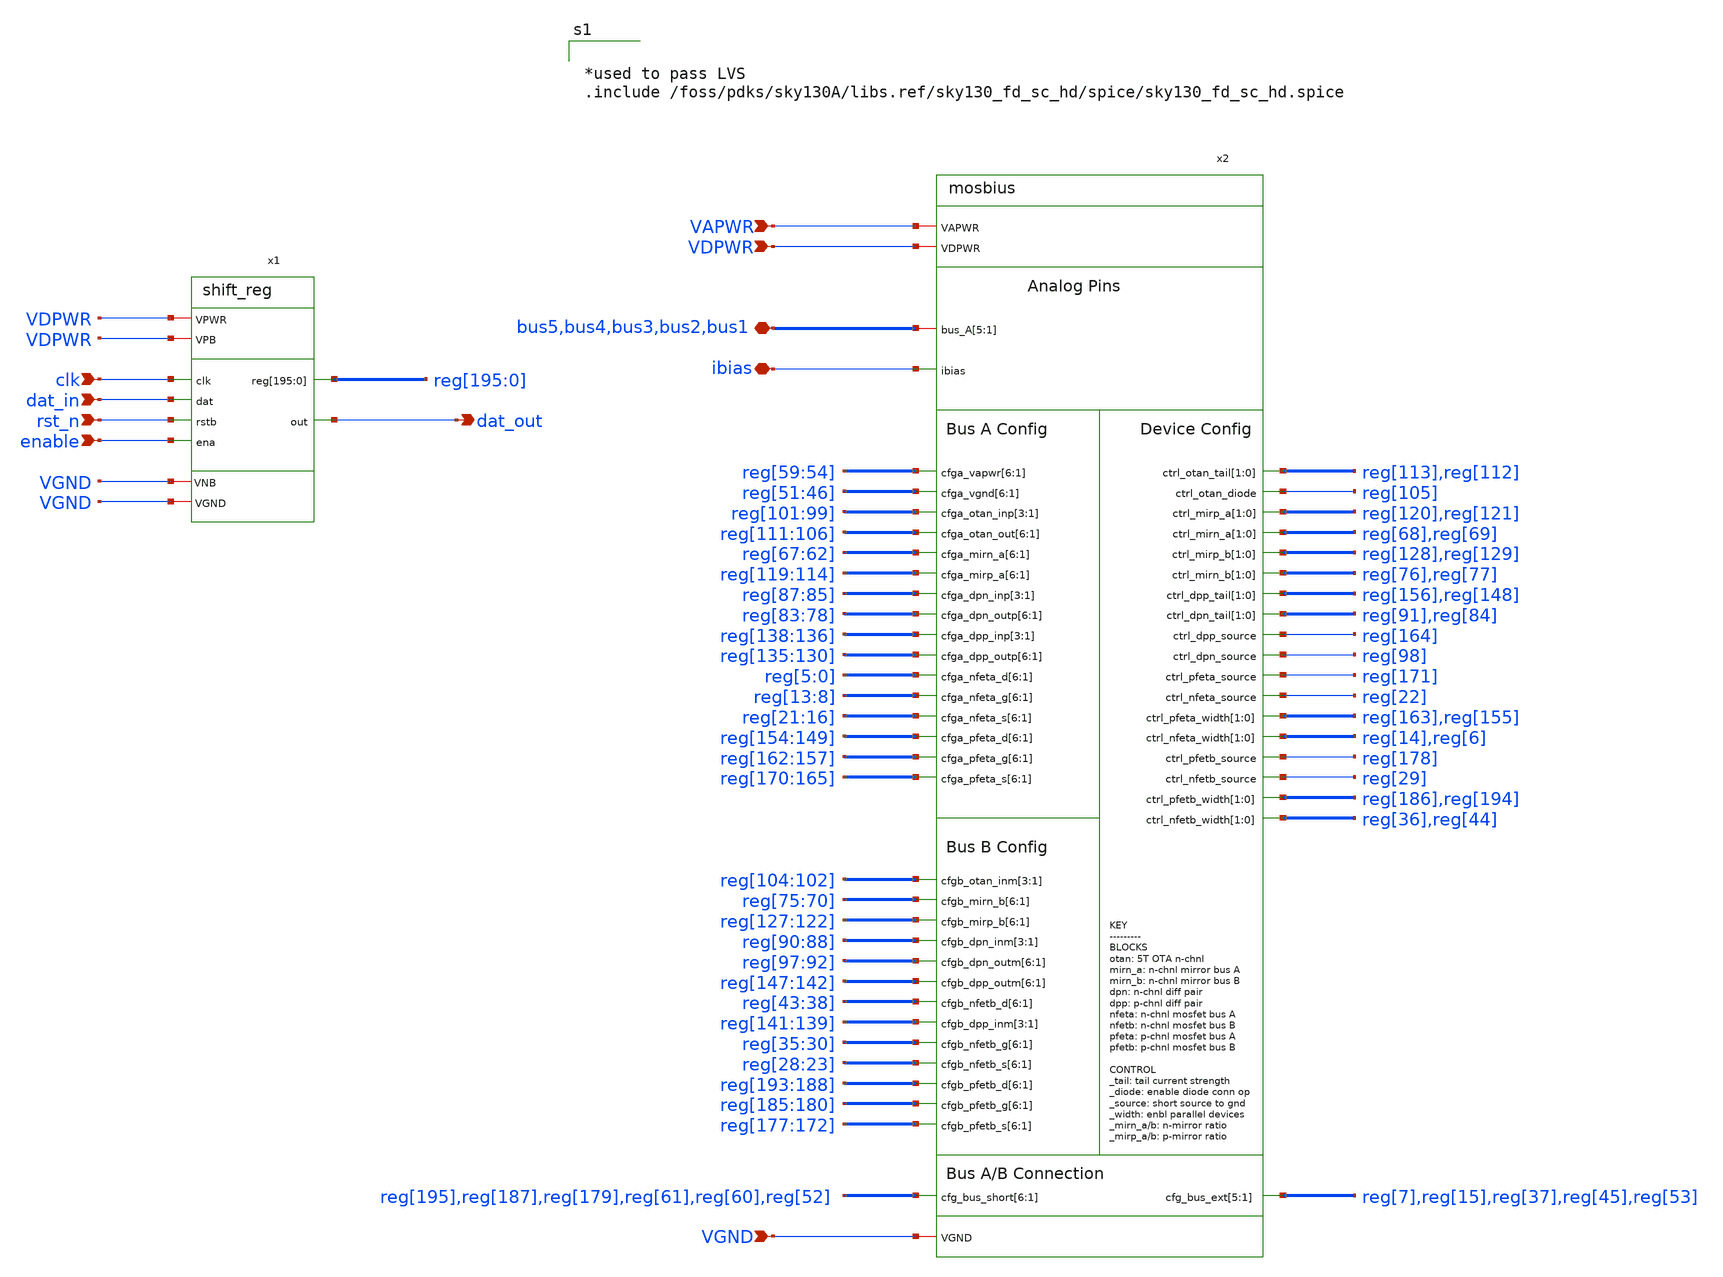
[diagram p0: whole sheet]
** sch_path: tt_um_mosbius/xschem/tt_um_mosbius.sch
**.subckt tt_um_mosbius bus5,bus4,bus3,bus2,bus1 ibias VAPWR VDPWR VGND clk dat_in rst_n dat_out
*+ enable
*.iopin bus5,bus4,bus3,bus2,bus1
*.iopin ibias
*.ipin VAPWR
*.ipin VDPWR
*.ipin VGND
*.ipin clk
*.ipin dat_in
*.ipin rst_n
*.opin dat_out
*.ipin enable
x2 reg[59] reg[58] reg[57] reg[56] reg[55] reg[54] VAPWR reg[51] reg[50] reg[49] reg[48] reg[47]
+ reg[46] VDPWR VGND bus5 bus4 bus3 bus2 bus1 reg[101] reg[100] reg[99] reg[104] reg[103] reg[102] reg[111]
+ reg[110] reg[109] reg[108] reg[107] reg[106] reg[67] reg[66] reg[65] reg[64] reg[63] reg[62] reg[75] reg[74]
+ reg[73] reg[72] reg[71] reg[70] reg[113] reg[112] reg[105] reg[119] reg[118] reg[117] reg[116] reg[115]
+ reg[114] reg[127] reg[126] reg[125] reg[124] reg[123] reg[122] reg[87] reg[86] reg[85] reg[90] reg[89]
+ reg[88] reg[83] reg[82] reg[81] reg[80] reg[79] reg[78] ibias reg[97] reg[96] reg[95] reg[94] reg[93]
+ reg[92] reg[120] reg[121] reg[68] reg[69] reg[128] reg[129] reg[76] reg[77] reg[138] reg[137] reg[136]
+ reg[141] reg[140] reg[139] reg[135] reg[134] reg[133] reg[132] reg[131] reg[130] reg[147] reg[146] reg[145]
+ reg[144] reg[143] reg[142] reg[5] reg[4] reg[3] reg[2] reg[1] reg[0] reg[43] reg[42] reg[41] reg[40] reg[39]
+ reg[38] reg[13] reg[12] reg[11] reg[10] reg[9] reg[8] reg[156] reg[148] reg[91] reg[84] reg[35] reg[34]
+ reg[33] reg[32] reg[31] reg[30] reg[164] reg[98] reg[21] reg[20] reg[19] reg[18] reg[17] reg[16] reg[28]
+ reg[27] reg[26] reg[25] reg[24] reg[23] reg[154] reg[153] reg[152] reg[151] reg[150] reg[149] reg[193]
+ reg[192] reg[191] reg[190] reg[189] reg[188] reg[162] reg[161] reg[160] reg[159] reg[158] reg[157] reg[171]
+ reg[22] reg[185] reg[184] reg[183] reg[182] reg[181] reg[180] reg[163] reg[155] reg[14] reg[6] reg[170]
+ reg[169] reg[168] reg[167] reg[166] reg[165] reg[177] reg[176] reg[175] reg[174] reg[173] reg[172] reg[178]
+ reg[29] reg[186] reg[194] reg[36] reg[44] reg[195] reg[187] reg[179] reg[61] reg[60] reg[52] reg[7] reg[15]
+ reg[37] reg[45] reg[53] mosbius
x1 VDPWR dat_in enable clk rst_n VGND reg[195] reg[194] reg[193] reg[192] reg[191] reg[190] reg[189]
+ reg[188] reg[187] reg[186] reg[185] reg[184] reg[183] reg[182] reg[181] reg[180] reg[179] reg[178] reg[177]
+ reg[176] reg[175] reg[174] reg[173] reg[172] reg[171] reg[170] reg[169] reg[168] reg[167] reg[166] reg[165]
+ reg[164] reg[163] reg[162] reg[161] reg[160] reg[159] reg[158] reg[157] reg[156] reg[155] reg[154] reg[153]
+ reg[152] reg[151] reg[150] reg[149] reg[148] reg[147] reg[146] reg[145] reg[144] reg[143] reg[142] reg[141]
+ reg[140] reg[139] reg[138] reg[137] reg[136] reg[135] reg[134] reg[133] reg[132] reg[131] reg[130] reg[129]
+ reg[128] reg[127] reg[126] reg[125] reg[124] reg[123] reg[122] reg[121] reg[120] reg[119] reg[118] reg[117]
+ reg[116] reg[115] reg[114] reg[113] reg[112] reg[111] reg[110] reg[109] reg[108] reg[107] reg[106] reg[105]
+ reg[104] reg[103] reg[102] reg[101] reg[100] reg[99] reg[98] reg[97] reg[96] reg[95] reg[94] reg[93] reg[92]
+ reg[91] reg[90] reg[89] reg[88] reg[87] reg[86] reg[85] reg[84] reg[83] reg[82] reg[81] reg[80] reg[79]
+ reg[78] reg[77] reg[76] reg[75] reg[74] reg[73] reg[72] reg[71] reg[70] reg[69] reg[68] reg[67] reg[66]
+ reg[65] reg[64] reg[63] reg[62] reg[61] reg[60] reg[59] reg[58] reg[57] reg[56] reg[55] reg[54] reg[53]
+ reg[52] reg[51] reg[50] reg[49] reg[48] reg[47] reg[46] reg[45] reg[44] reg[43] reg[42] reg[41] reg[40]
+ reg[39] reg[38] reg[37] reg[36] reg[35] reg[34] reg[33] reg[32] reg[31] reg[30] reg[29] reg[28] reg[27]
+ reg[26] reg[25] reg[24] reg[23] reg[22] reg[21] reg[20] reg[19] reg[18] reg[17] reg[16] reg[15] reg[14]
+ reg[13] reg[12] reg[11] reg[10] reg[9] reg[8] reg[7] reg[6] reg[5] reg[4] reg[3] reg[2] reg[1] reg[0]
+ dat_out VGND VDPWR shift_reg
**** begin user architecture code


*used to pass LVS
.include /foss/pdks/sky130A/libs.ref/sky130_fd_sc_hd/spice/sky130_fd_sc_hd.spice


**** end user architecture code
**.ends
.end
